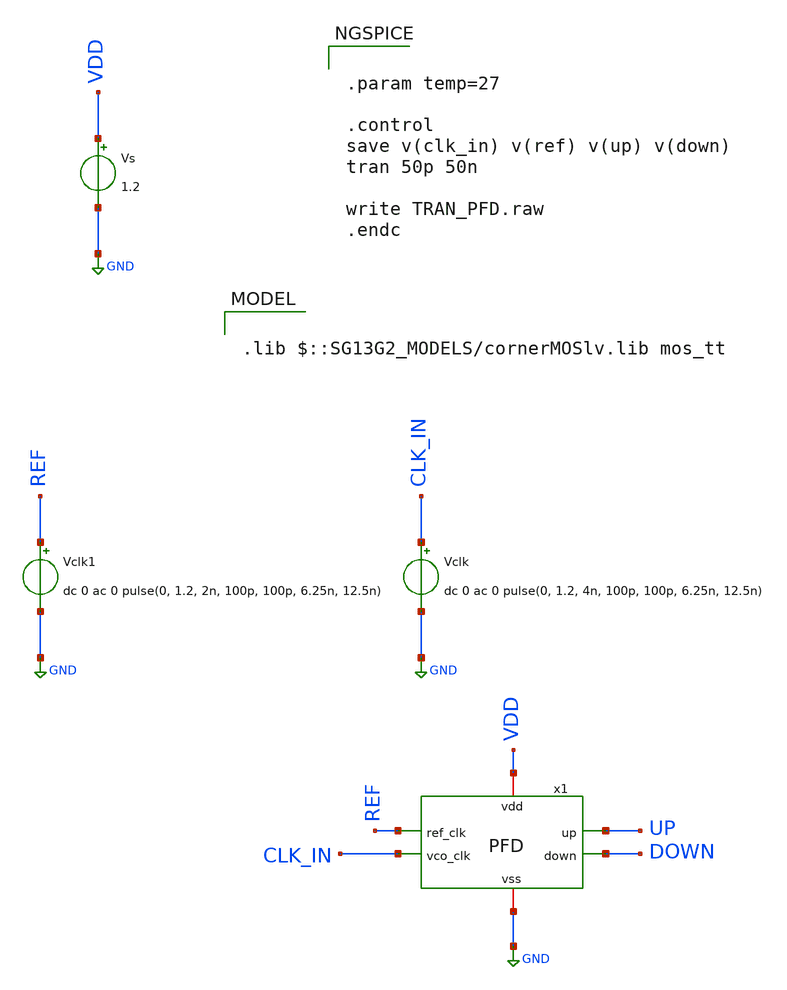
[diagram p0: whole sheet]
** sch_path: 30_MHz_Fractional_N_PLL/design_data/xschem/PFD_TB.sch

.lib $::SG13G2_MODELS/cornerMOSlv.lib mos_tt

**.subckt PFD_TB
Vs VDD GND 1.2
Vclk CLK_IN GND dc 0 ac 0 pulse(0, 1.2, 4n, 100p, 100p, 6.25n, 12.5n)
x1 VDD UP GND DOWN REF CLK_IN PFD
Vclk1 REF GND dc 0 ac 0 pulse(0, 1.2, 2n, 100p, 100p, 6.25n, 12.5n)
**** begin user architecture code


.param temp=27

.control
save v(clk_in) v(ref) v(up) v(down)
tran 50p 50n

write TRAN_PFD.raw
.endc


**** end user architecture code
**.ends

* expanding   symbol:  PFD.sym # of pins=6
** sym_path: 30_MHz_Fractional_N_PLL/design_data/xschem/PFD.sym
** sch_path: 30_MHz_Fractional_N_PLL/design_data/xschem/PFD.sch
.subckt PFD vdd up vss down ref_clk vco_clk
*.iopin vdd
*.ipin ref_clk
*.iopin vss
*.ipin vco_clk
*.opin up
*.opin down
XM1 net2 vco_clk vss vss sg13_lv_nmos w=0.36u l=0.15u ng=1 m=1 mm_ok=1
XM4 net1 ref_clk net2 vss sg13_lv_nmos w=1.8u l=0.15u ng=1 m=1 mm_ok=1
XM5 net3 ref_clk net1 vss sg13_lv_nmos w=0.84u l=0.15u ng=1 m=1 mm_ok=1
XM9 net3 ref_clk ref_clk vdd sg13_lv_pmos w=0.64u l=0.15u ng=1 m=1 mm_ok=1
XM11 net7 net3 vss vss sg13_lv_nmos w=0.36u l=0.15u ng=1 m=1 mm_ok=1
XM12 vdd net3 net7 vdd sg13_lv_pmos w=0.72u l=0.15u ng=1 m=1 mm_ok=1
XM13 up net7 vss vss sg13_lv_nmos w=0.48u l=0.15u ng=1 m=1 mm_ok=1
XM14 vdd net7 up vdd sg13_lv_pmos w=0.96u l=0.15u ng=1 m=1 mm_ok=1
XM3 net1 ref_clk vdd vdd sg13_lv_pmos w=0.64u l=0.15u ng=1 m=1 mm_ok=1
XM6 net4 vco_clk vdd vdd sg13_lv_pmos w=0.64u l=0.15u ng=1 m=1 mm_ok=1
XM7 net4 vco_clk net5 vss sg13_lv_nmos w=1.8u l=0.15u ng=1 m=1 mm_ok=1
XM19 net5 ref_clk vss vss sg13_lv_nmos w=0.36u l=0.15u ng=1 m=1 mm_ok=1
XM8 net6 vco_clk net4 vss sg13_lv_nmos w=0.84u l=0.15u ng=1 m=1 mm_ok=1
XM10 net6 vco_clk vco_clk vdd sg13_lv_pmos w=0.64u l=0.15u ng=1 m=1 mm_ok=1
XM15 vdd net6 net8 vdd sg13_lv_pmos w=0.72u l=0.15u ng=1 m=1 mm_ok=1
XM16 net8 net6 vss vss sg13_lv_nmos w=0.36u l=0.15u ng=1 m=1 mm_ok=1
XM17 vdd net8 down vdd sg13_lv_pmos w=0.96u l=0.15u ng=1 m=1 mm_ok=1
XM18 down net8 vss vss sg13_lv_nmos w=0.48u l=0.15u ng=1 m=1 mm_ok=1
.ends

.GLOBAL GND
.end
